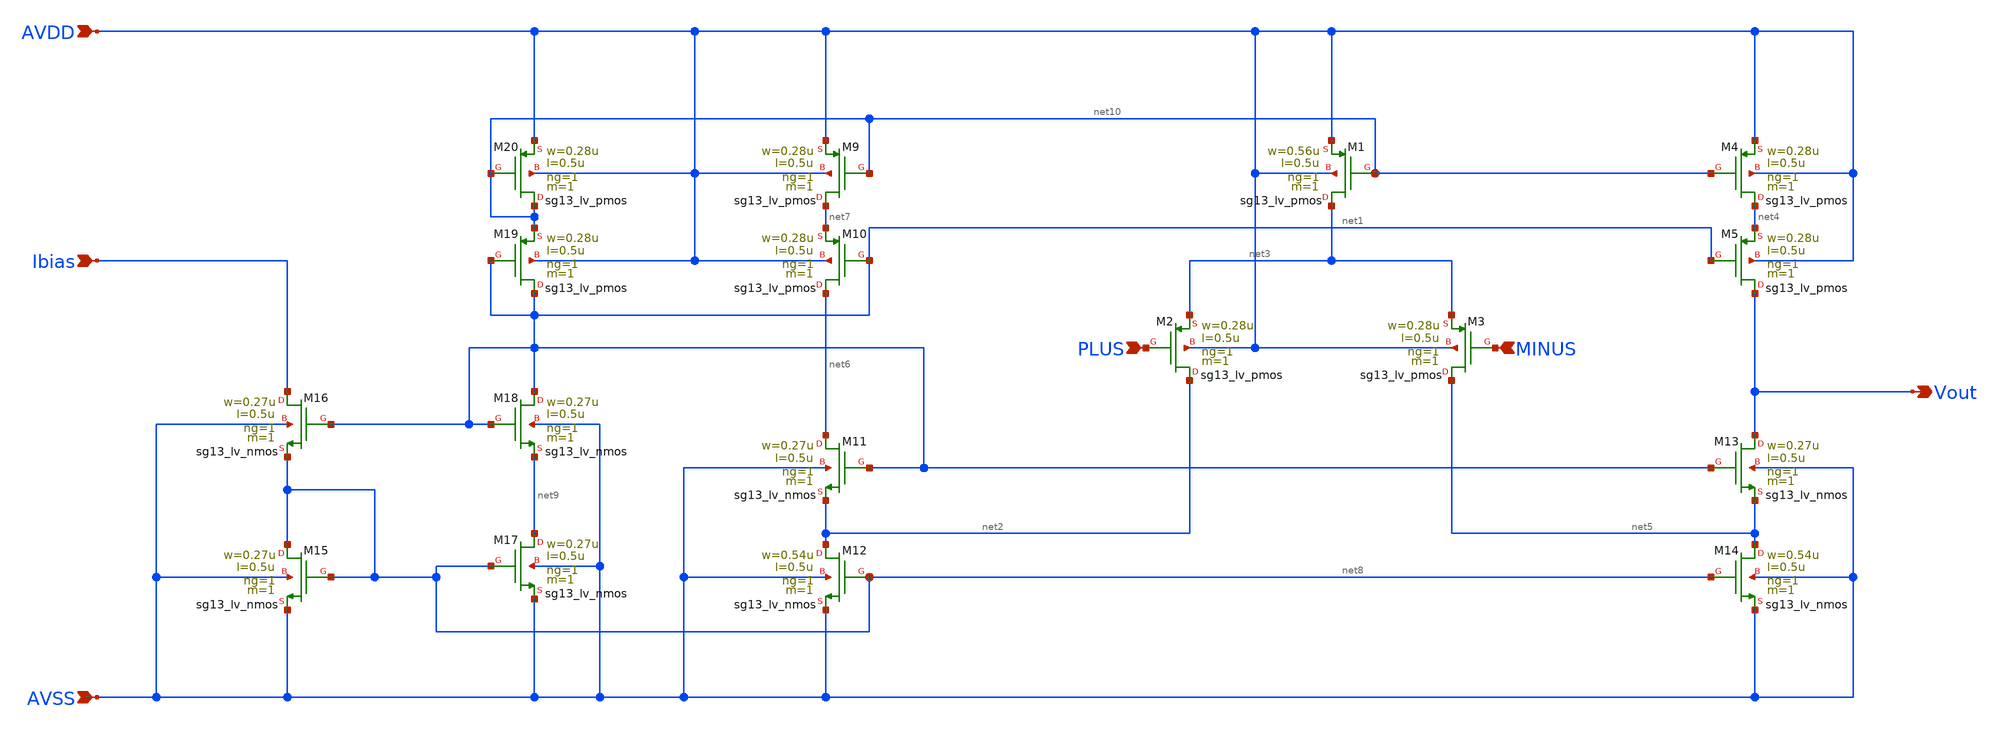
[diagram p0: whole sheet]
** sch_path: Designs/otas/foldedcascode.sch
* (c) 2025 Thesis_HP, Apache-2.0 license
**.subckt foldedcascode PLUS MINUS Vout AVDD AVSS Ibias
*.ipin PLUS
*.ipin MINUS
*.opin Vout
*.ipin AVDD
*.ipin AVSS
*.ipin Ibias
XM1 net3 net10 AVDD AVDD sg13_lv_pmos w=0.56u l=0.5u ng=1 m=1 mm_ok=1
XM2 net2 PLUS net3 AVDD sg13_lv_pmos w=0.28u l=0.5u ng=1 m=1 mm_ok=1
XM3 net5 MINUS net3 AVDD sg13_lv_pmos w=0.28u l=0.5u ng=1 m=1 mm_ok=1
XM4 net4 net10 AVDD AVDD sg13_lv_pmos w=0.28u l=0.5u ng=1 m=1 mm_ok=1
XM5 Vout net1 net4 AVDD sg13_lv_pmos w=0.28u l=0.5u ng=1 m=1 mm_ok=1
XM14 net5 net8 AVSS AVSS sg13_lv_nmos w=0.54u l=0.5u ng=1 m=1 mm_ok=1
XM13 Vout net1 net5 AVSS sg13_lv_nmos w=0.27u l=0.5u ng=1 m=1 mm_ok=1
XM11 net6 net1 net2 AVSS sg13_lv_nmos w=0.27u l=0.5u ng=1 m=1 mm_ok=1
XM12 net2 net8 AVSS AVSS sg13_lv_nmos w=0.54u l=0.5u ng=1 m=1 mm_ok=1
XM17 net9 net8 AVSS AVSS sg13_lv_nmos w=0.27u l=0.5u ng=1 m=1 mm_ok=1
XM18 net1 net1 net9 AVSS sg13_lv_nmos w=0.27u l=0.5u ng=1 m=1 mm_ok=1
XM16 Ibias net1 net8 AVSS sg13_lv_nmos w=0.27u l=0.5u ng=1 m=1 mm_ok=1
XM15 net8 net8 AVSS AVSS sg13_lv_nmos w=0.27u l=0.5u ng=1 m=1 mm_ok=1
XM10 net6 net1 net7 AVDD sg13_lv_pmos w=0.28u l=0.5u ng=1 m=1 mm_ok=1
XM9 net7 net10 AVDD AVDD sg13_lv_pmos w=0.28u l=0.5u ng=1 m=1 mm_ok=1
XM19 net1 net1 net10 AVDD sg13_lv_pmos w=0.28u l=0.5u ng=1 m=1 mm_ok=1
XM20 net10 net10 AVDD AVDD sg13_lv_pmos w=0.28u l=0.5u ng=1 m=1 mm_ok=1
**.ends
.end
